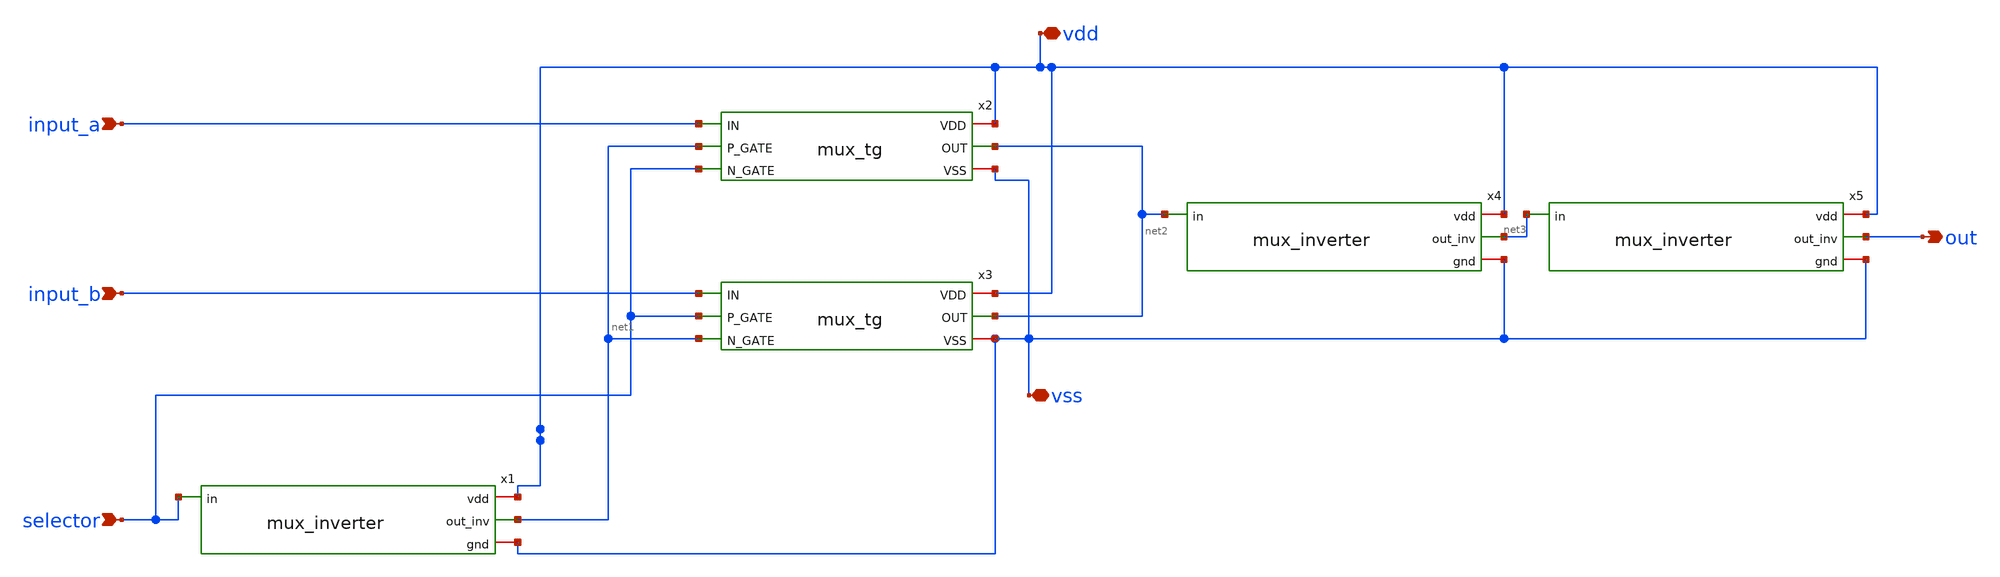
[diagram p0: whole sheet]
** sch_path: designs/digital/clb_mosbius/mux2x1_transmission_gate/mux_toplevel.sch
**.subckt mux_toplevel vdd out input_a input_b selector vss
*.iopin vdd
*.opin out
*.ipin input_a
*.ipin input_b
*.ipin selector
*.iopin vss
x2 vdd net1 input_a net2 selector vss mux_tg
x1 vdd selector net1 vss mux_inverter
x3 vdd selector input_b net2 net1 vss mux_tg
x4 vdd net2 net3 vss mux_inverter
x5 vdd net3 out vss mux_inverter
**.ends
.end
